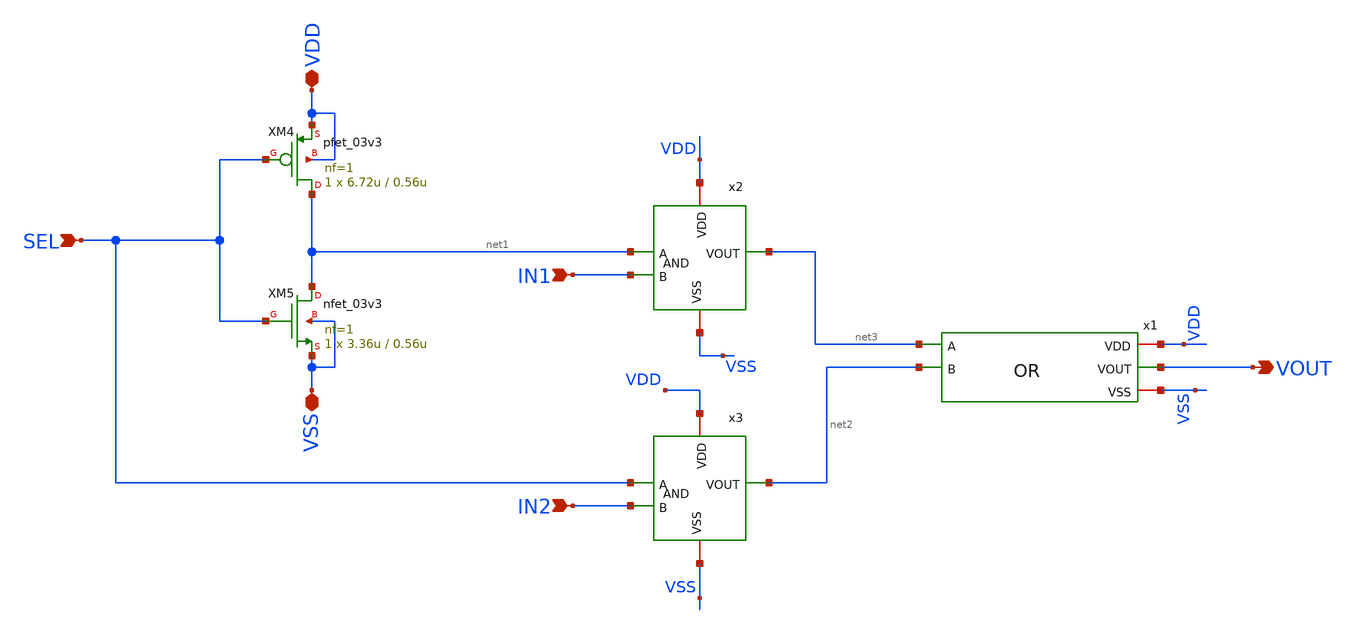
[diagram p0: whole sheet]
** sch_path: PLL-main/schematic/xschem/MUX.sch
**.subckt MUX SEL IN1 IN2 VOUT VDD VSS
*.ipin SEL
*.ipin IN1
*.ipin IN2
*.opin VOUT
*.iopin VDD
*.iopin VSS
x2 VDD net3 net1 IN1 VSS AND
x3 VDD net2 SEL IN2 VSS AND
XM4 net1 SEL VDD VDD pfet_03v3 L=0.56u W=6.72u nf=1 ad='int((nf+1)/2) * W/nf * 0.18u' as='int((nf+2)/2) * W/nf * 0.18u'
+ pd='2*int((nf+1)/2) * (W/nf + 0.18u)' ps='2*int((nf+2)/2) * (W/nf + 0.18u)' nrd='0.18u / W' nrs='0.18u / W'
+ sa=0 sb=0 sd=0 m=1
XM5 net1 SEL VSS VSS nfet_03v3 L=0.56u W=3.36u nf=1 ad='int((nf+1)/2) * W/nf * 0.18u' as='int((nf+2)/2) * W/nf * 0.18u'
+ pd='2*int((nf+1)/2) * (W/nf + 0.18u)' ps='2*int((nf+2)/2) * (W/nf + 0.18u)' nrd='0.18u / W' nrs='0.18u / W'
+ sa=0 sb=0 sd=0 m=1
x1 VDD net3 net2 VOUT VSS OR
**.ends

* expanding   symbol:  AND.sym # of pins=5
** sym_path: AND.sym
** sch_path: AND.sch
.subckt AND VDD VOUT A B VSS
*.iopin VDD
*.iopin VSS
*.ipin A
*.ipin B
*.opin VOUT
XM1 net1 A net2 VSS nfet_03v3 L=0.56u W=2.24u nf=1 ad='int((nf+1)/2) * W/nf * 0.18u' as='int((nf+2)/2) * W/nf * 0.18u'
+ pd='2*int((nf+1)/2) * (W/nf + 0.18u)' ps='2*int((nf+2)/2) * (W/nf + 0.18u)' nrd='0.18u / W' nrs='0.18u / W'
+ sa=0 sb=0 sd=0 m=1
XM2 net1 A VDD VDD pfet_03v3 L=0.56u W=2.24u nf=1 ad='int((nf+1)/2) * W/nf * 0.18u' as='int((nf+2)/2) * W/nf * 0.18u'
+ pd='2*int((nf+1)/2) * (W/nf + 0.18u)' ps='2*int((nf+2)/2) * (W/nf + 0.18u)' nrd='0.18u / W' nrs='0.18u / W'
+ sa=0 sb=0 sd=0 m=1
XM3 net1 B VDD VDD pfet_03v3 L=0.56u W=2.24u nf=1 ad='int((nf+1)/2) * W/nf * 0.18u' as='int((nf+2)/2) * W/nf * 0.18u'
+ pd='2*int((nf+1)/2) * (W/nf + 0.18u)' ps='2*int((nf+2)/2) * (W/nf + 0.18u)' nrd='0.18u / W' nrs='0.18u / W'
+ sa=0 sb=0 sd=0 m=1
XM4 net2 B VSS VSS nfet_03v3 L=0.56u W=2.24u nf=1 ad='int((nf+1)/2) * W/nf * 0.18u' as='int((nf+2)/2) * W/nf * 0.18u'
+ pd='2*int((nf+1)/2) * (W/nf + 0.18u)' ps='2*int((nf+2)/2) * (W/nf + 0.18u)' nrd='0.18u / W' nrs='0.18u / W'
+ sa=0 sb=0 sd=0 m=1
XM5 VOUT net1 VDD VDD pfet_03v3 L=0.56u W=2.24u nf=1 ad='int((nf+1)/2) * W/nf * 0.18u' as='int((nf+2)/2) * W/nf * 0.18u'
+ pd='2*int((nf+1)/2) * (W/nf + 0.18u)' ps='2*int((nf+2)/2) * (W/nf + 0.18u)' nrd='0.18u / W' nrs='0.18u / W'
+ sa=0 sb=0 sd=0 m=1
XM6 VOUT net1 VSS VSS nfet_03v3 L=0.56u W=1.12u nf=1 ad='int((nf+1)/2) * W/nf * 0.18u' as='int((nf+2)/2) * W/nf * 0.18u'
+ pd='2*int((nf+1)/2) * (W/nf + 0.18u)' ps='2*int((nf+2)/2) * (W/nf + 0.18u)' nrd='0.18u / W' nrs='0.18u / W'
+ sa=0 sb=0 sd=0 m=1
.ends


* expanding   symbol:  OR.sym # of pins=5
** sym_path: PLL-main/schematic/xschem/OR.sym
** sch_path: PLL-main/schematic/xschem/OR.sch
.subckt OR VDD A B VOUT VSS
*.iopin VSS
*.iopin VDD
*.ipin A
*.ipin B
*.opin VOUT
XM1 net1 A VSS VSS nfet_03v3 L=0.56u W=1.12u nf=1 ad='int((nf+1)/2) * W/nf * 0.18u' as='int((nf+2)/2) * W/nf * 0.18u'
+ pd='2*int((nf+1)/2) * (W/nf + 0.18u)' ps='2*int((nf+2)/2) * (W/nf + 0.18u)' nrd='0.18u / W' nrs='0.18u / W'
+ sa=0 sb=0 sd=0 m=1
XM2 net1 B net2 VDD pfet_03v3 L=0.56u W=4.48u nf=1 ad='int((nf+1)/2) * W/nf * 0.18u' as='int((nf+2)/2) * W/nf * 0.18u'
+ pd='2*int((nf+1)/2) * (W/nf + 0.18u)' ps='2*int((nf+2)/2) * (W/nf + 0.18u)' nrd='0.18u / W' nrs='0.18u / W'
+ sa=0 sb=0 sd=0 m=1
XM3 net1 B VSS VSS nfet_03v3 L=0.56u W=1.12u nf=1 ad='int((nf+1)/2) * W/nf * 0.18u' as='int((nf+2)/2) * W/nf * 0.18u'
+ pd='2*int((nf+1)/2) * (W/nf + 0.18u)' ps='2*int((nf+2)/2) * (W/nf + 0.18u)' nrd='0.18u / W' nrs='0.18u / W'
+ sa=0 sb=0 sd=0 m=1
XM6 net2 A VDD VDD pfet_03v3 L=0.56u W=4.48u nf=1 ad='int((nf+1)/2) * W/nf * 0.18u' as='int((nf+2)/2) * W/nf * 0.18u'
+ pd='2*int((nf+1)/2) * (W/nf + 0.18u)' ps='2*int((nf+2)/2) * (W/nf + 0.18u)' nrd='0.18u / W' nrs='0.18u / W'
+ sa=0 sb=0 sd=0 m=1
XM4 VOUT net1 VDD VDD pfet_03v3 L=0.56u W=2.24u nf=1 ad='int((nf+1)/2) * W/nf * 0.18u' as='int((nf+2)/2) * W/nf * 0.18u'
+ pd='2*int((nf+1)/2) * (W/nf + 0.18u)' ps='2*int((nf+2)/2) * (W/nf + 0.18u)' nrd='0.18u / W' nrs='0.18u / W'
+ sa=0 sb=0 sd=0 m=1
XM5 VOUT net1 VSS VSS nfet_03v3 L=0.56u W=1.12u nf=1 ad='int((nf+1)/2) * W/nf * 0.18u' as='int((nf+2)/2) * W/nf * 0.18u'
+ pd='2*int((nf+1)/2) * (W/nf + 0.18u)' ps='2*int((nf+2)/2) * (W/nf + 0.18u)' nrd='0.18u / W' nrs='0.18u / W'
+ sa=0 sb=0 sd=0 m=1
.ends

.end
